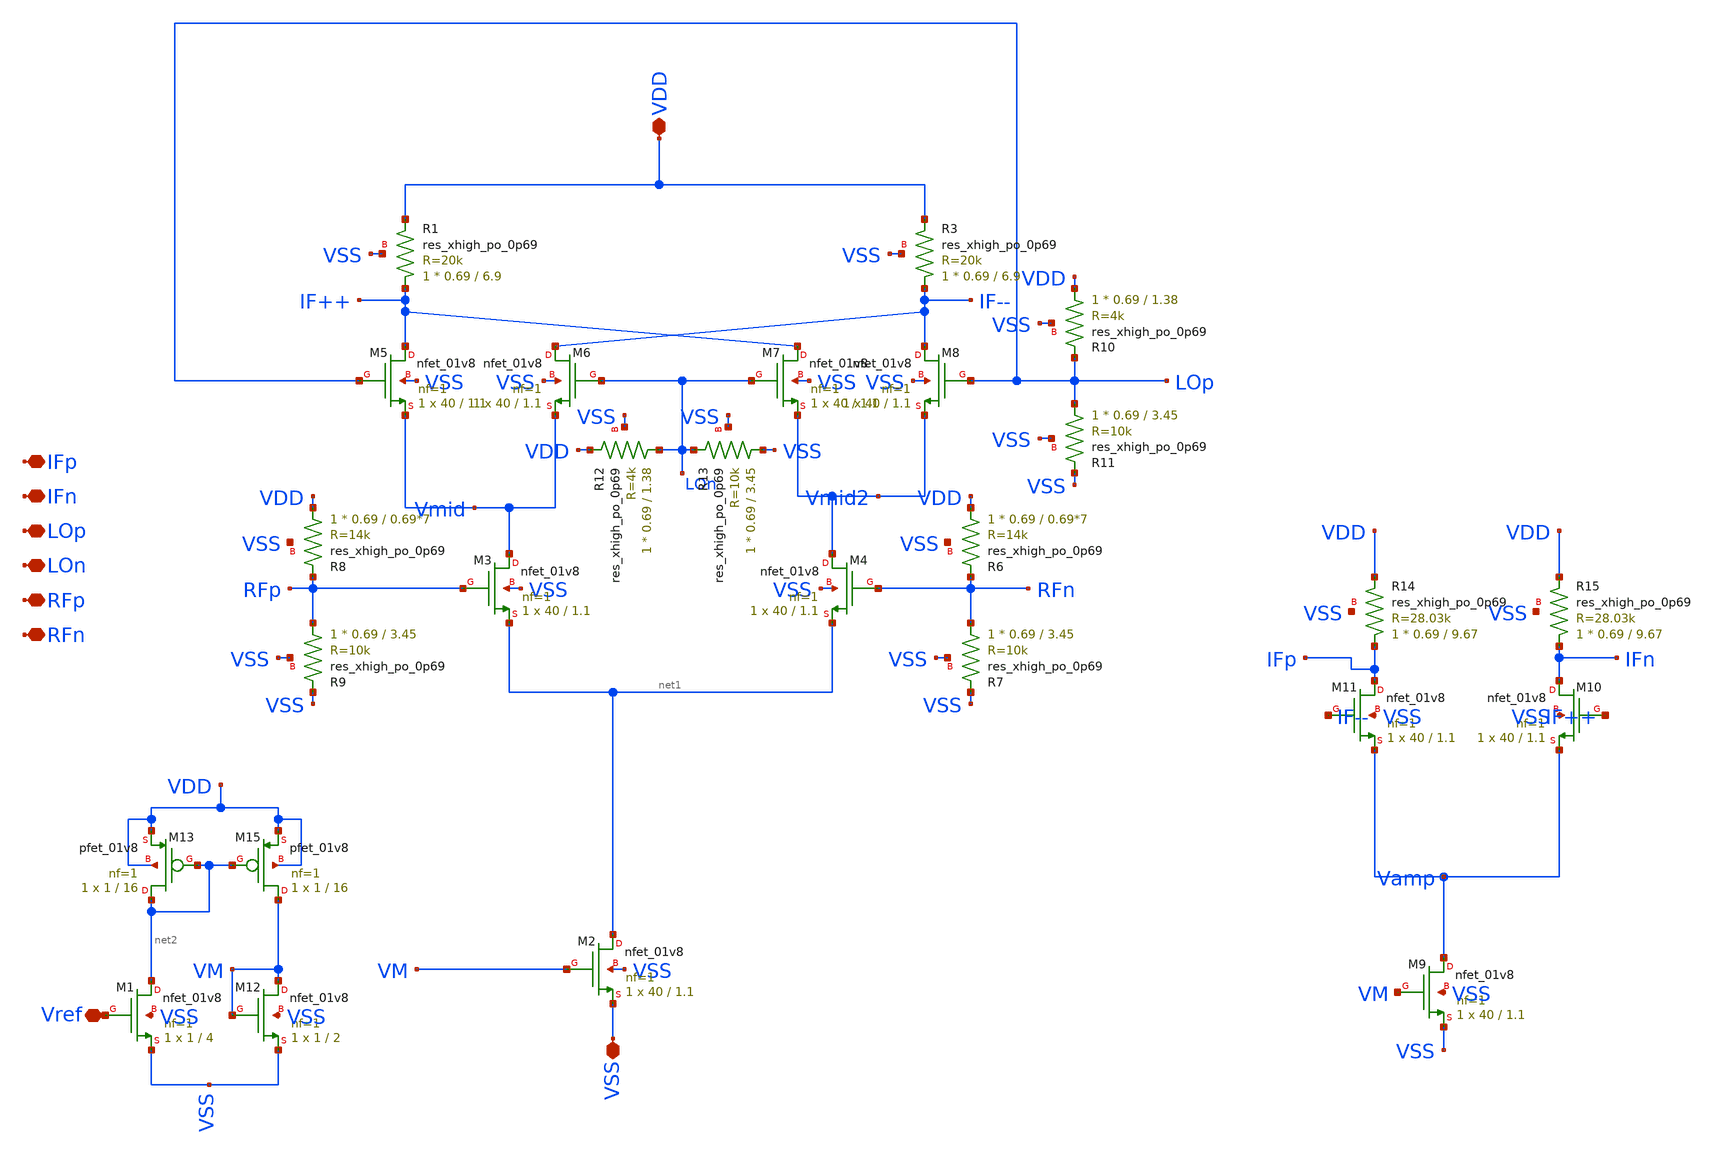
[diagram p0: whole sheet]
** sch_path: hw07/xschem/gill_cell.sch
**.subckt gill_cell IFp IFn LOp LOn RFp RFn VDD VSS Vref
*.iopin IFp
*.iopin IFn
*.iopin LOp
*.iopin LOn
*.iopin RFp
*.iopin RFn
*.iopin VDD
*.iopin VSS
*.iopin Vref
XR1 IF++ VDD VSS sky130_fd_pr__res_xhigh_po_0p69 L=6.9 mult=1 m=1
XR3 IF-- VDD VSS sky130_fd_pr__res_xhigh_po_0p69 L=6.9 mult=1 m=1
XR10 VDD LOp VSS sky130_fd_pr__res_xhigh_po_0p69 L=1.38 mult=1 m=1
XR11 LOp VSS VSS sky130_fd_pr__res_xhigh_po_0p69 L=3.45 mult=1 m=1
XR6 VDD RFn VSS sky130_fd_pr__res_xhigh_po_0p69 L=0.69*7 mult=1 m=1
XR7 RFn VSS VSS sky130_fd_pr__res_xhigh_po_0p69 L=3.45 mult=1 m=1
XR8 VDD RFp VSS sky130_fd_pr__res_xhigh_po_0p69 L=0.69*7 mult=1 m=1
XR9 RFp VSS VSS sky130_fd_pr__res_xhigh_po_0p69 L=3.45 mult=1 m=1
XR12 LOn VDD VSS sky130_fd_pr__res_xhigh_po_0p69 L=1.38 mult=1 m=1
XR13 VSS LOn VSS sky130_fd_pr__res_xhigh_po_0p69 L=3.45 mult=1 m=1
XM2 net1 VM VSS VSS sky130_fd_pr__nfet_01v8 L=1.1 W=40 nf=1 ad='int((nf+1)/2) * W/nf * 0.29' as='int((nf+2)/2) * W/nf * 0.29'
+ pd='2*int((nf+1)/2) * (W/nf + 0.29)' ps='2*int((nf+2)/2) * (W/nf + 0.29)' nrd='0.29 / W' nrs='0.29 / W'
+ sa=0 sb=0 sd=0 mult=1 m=1
XM3 Vmid RFp net1 VSS sky130_fd_pr__nfet_01v8 L=1.1 W=40 nf=1 ad='int((nf+1)/2) * W/nf * 0.29' as='int((nf+2)/2) * W/nf * 0.29'
+ pd='2*int((nf+1)/2) * (W/nf + 0.29)' ps='2*int((nf+2)/2) * (W/nf + 0.29)' nrd='0.29 / W' nrs='0.29 / W'
+ sa=0 sb=0 sd=0 mult=1 m=1
XM5 IF++ LOp Vmid VSS sky130_fd_pr__nfet_01v8 L=1.1 W=40 nf=1 ad='int((nf+1)/2) * W/nf * 0.29' as='int((nf+2)/2) * W/nf * 0.29'
+ pd='2*int((nf+1)/2) * (W/nf + 0.29)' ps='2*int((nf+2)/2) * (W/nf + 0.29)' nrd='0.29 / W' nrs='0.29 / W'
+ sa=0 sb=0 sd=0 mult=1 m=1
XM7 IF++ LOn Vmid2 VSS sky130_fd_pr__nfet_01v8 L=1.1 W=40 nf=1 ad='int((nf+1)/2) * W/nf * 0.29' as='int((nf+2)/2) * W/nf * 0.29'
+ pd='2*int((nf+1)/2) * (W/nf + 0.29)' ps='2*int((nf+2)/2) * (W/nf + 0.29)' nrd='0.29 / W' nrs='0.29 / W'
+ sa=0 sb=0 sd=0 mult=1 m=1
XM4 Vmid2 RFn net1 VSS sky130_fd_pr__nfet_01v8 L=1.1 W=40 nf=1 ad='int((nf+1)/2) * W/nf * 0.29' as='int((nf+2)/2) * W/nf * 0.29'
+ pd='2*int((nf+1)/2) * (W/nf + 0.29)' ps='2*int((nf+2)/2) * (W/nf + 0.29)' nrd='0.29 / W' nrs='0.29 / W'
+ sa=0 sb=0 sd=0 mult=1 m=1
XM8 IF-- LOp Vmid2 VSS sky130_fd_pr__nfet_01v8 L=1.1 W=40 nf=1 ad='int((nf+1)/2) * W/nf * 0.29' as='int((nf+2)/2) * W/nf * 0.29'
+ pd='2*int((nf+1)/2) * (W/nf + 0.29)' ps='2*int((nf+2)/2) * (W/nf + 0.29)' nrd='0.29 / W' nrs='0.29 / W'
+ sa=0 sb=0 sd=0 mult=1 m=1
XM6 IF-- LOn Vmid VSS sky130_fd_pr__nfet_01v8 L=1.1 W=40 nf=1 ad='int((nf+1)/2) * W/nf * 0.29' as='int((nf+2)/2) * W/nf * 0.29'
+ pd='2*int((nf+1)/2) * (W/nf + 0.29)' ps='2*int((nf+2)/2) * (W/nf + 0.29)' nrd='0.29 / W' nrs='0.29 / W'
+ sa=0 sb=0 sd=0 mult=1 m=1
XM9 Vamp VM VSS VSS sky130_fd_pr__nfet_01v8 L=1.1 W=40 nf=1 ad='int((nf+1)/2) * W/nf * 0.29' as='int((nf+2)/2) * W/nf * 0.29'
+ pd='2*int((nf+1)/2) * (W/nf + 0.29)' ps='2*int((nf+2)/2) * (W/nf + 0.29)' nrd='0.29 / W' nrs='0.29 / W'
+ sa=0 sb=0 sd=0 mult=1 m=1
XM10 IFn IF++ Vamp VSS sky130_fd_pr__nfet_01v8 L=1.1 W=40 nf=1 ad='int((nf+1)/2) * W/nf * 0.29' as='int((nf+2)/2) * W/nf * 0.29'
+ pd='2*int((nf+1)/2) * (W/nf + 0.29)' ps='2*int((nf+2)/2) * (W/nf + 0.29)' nrd='0.29 / W' nrs='0.29 / W'
+ sa=0 sb=0 sd=0 mult=1 m=1
XM11 IFp IF-- Vamp VSS sky130_fd_pr__nfet_01v8 L=1.1 W=40 nf=1 ad='int((nf+1)/2) * W/nf * 0.29' as='int((nf+2)/2) * W/nf * 0.29'
+ pd='2*int((nf+1)/2) * (W/nf + 0.29)' ps='2*int((nf+2)/2) * (W/nf + 0.29)' nrd='0.29 / W' nrs='0.29 / W'
+ sa=0 sb=0 sd=0 mult=1 m=1
XR14 IFp VDD VSS sky130_fd_pr__res_xhigh_po_0p69 L=9.67 mult=1 m=1
XR15 IFn VDD VSS sky130_fd_pr__res_xhigh_po_0p69 L=9.67 mult=1 m=1
XM1 net2 Vref VSS VSS sky130_fd_pr__nfet_01v8 L=4 W=1 nf=1 ad='int((nf+1)/2) * W/nf * 0.29' as='int((nf+2)/2) * W/nf * 0.29'
+ pd='2*int((nf+1)/2) * (W/nf + 0.29)' ps='2*int((nf+2)/2) * (W/nf + 0.29)' nrd='0.29 / W' nrs='0.29 / W'
+ sa=0 sb=0 sd=0 mult=1 m=1
XM12 VM VM VSS VSS sky130_fd_pr__nfet_01v8 L=2 W=1 nf=1 ad='int((nf+1)/2) * W/nf * 0.29' as='int((nf+2)/2) * W/nf * 0.29'
+ pd='2*int((nf+1)/2) * (W/nf + 0.29)' ps='2*int((nf+2)/2) * (W/nf + 0.29)' nrd='0.29 / W' nrs='0.29 / W'
+ sa=0 sb=0 sd=0 mult=1 m=1
XM15 VM net2 VDD VDD sky130_fd_pr__pfet_01v8 L=16 W=1 nf=1 ad='int((nf+1)/2) * W/nf * 0.29' as='int((nf+2)/2) * W/nf * 0.29'
+ pd='2*int((nf+1)/2) * (W/nf + 0.29)' ps='2*int((nf+2)/2) * (W/nf + 0.29)' nrd='0.29 / W' nrs='0.29 / W'
+ sa=0 sb=0 sd=0 mult=1 m=1
XM13 net2 net2 VDD VDD sky130_fd_pr__pfet_01v8 L=16 W=1 nf=1 ad='int((nf+1)/2) * W/nf * 0.29' as='int((nf+2)/2) * W/nf * 0.29'
+ pd='2*int((nf+1)/2) * (W/nf + 0.29)' ps='2*int((nf+2)/2) * (W/nf + 0.29)' nrd='0.29 / W' nrs='0.29 / W'
+ sa=0 sb=0 sd=0 mult=1 m=1
**.ends
.end
